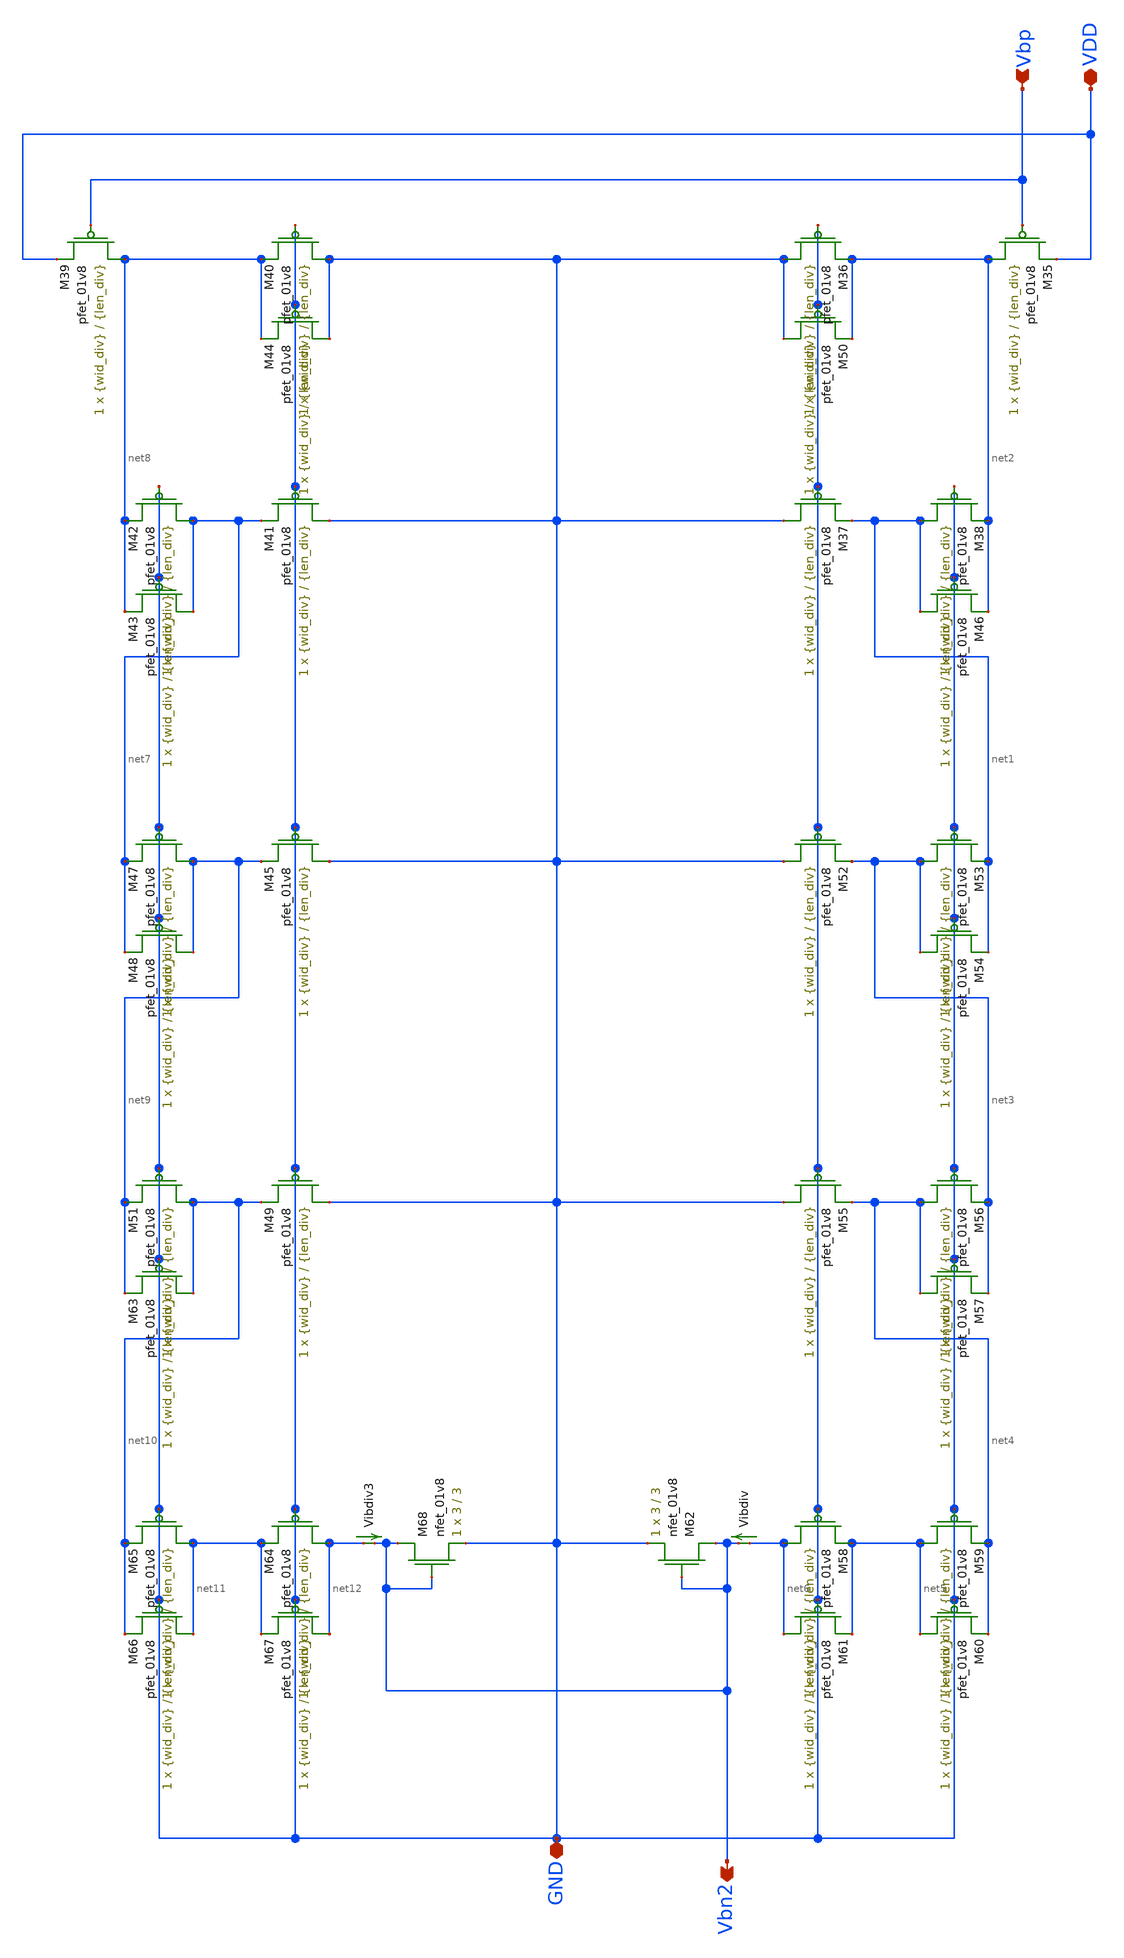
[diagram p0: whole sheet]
** sch_path: mp3/Layout_Schem_Designs/current_divider_lds.sch
**.subckt current_divider_lds Vbp VDD GND Vbn2
*.ipin Vbp
*.iopin VDD
*.iopin GND
*.opin Vbn2
XM35 net2 Vbp VDD VDD sky130_fd_pr__pfet_01v8 L={len_div} W={wid_div} nf=1 ad='int((nf+1)/2) * W/nf * 0.29'
+ as='int((nf+2)/2) * W/nf * 0.29' pd='2*int((nf+1)/2) * (W/nf + 0.29)' ps='2*int((nf+2)/2) * (W/nf + 0.29)'
+ nrd='0.29 / W' nrs='0.29 / W' sa=0 sb=0 sd=0 mult=1 m=1
XM36 GND GND net2 VDD sky130_fd_pr__pfet_01v8 L={len_div} W={wid_div} nf=1 ad='int((nf+1)/2) * W/nf * 0.29'
+ as='int((nf+2)/2) * W/nf * 0.29' pd='2*int((nf+1)/2) * (W/nf + 0.29)' ps='2*int((nf+2)/2) * (W/nf + 0.29)'
+ nrd='0.29 / W' nrs='0.29 / W' sa=0 sb=0 sd=0 mult=1 m=1
XM37 GND GND net1 VDD sky130_fd_pr__pfet_01v8 L={len_div} W={wid_div} nf=1 ad='int((nf+1)/2) * W/nf * 0.29'
+ as='int((nf+2)/2) * W/nf * 0.29' pd='2*int((nf+1)/2) * (W/nf + 0.29)' ps='2*int((nf+2)/2) * (W/nf + 0.29)'
+ nrd='0.29 / W' nrs='0.29 / W' sa=0 sb=0 sd=0 mult=1 m=1
XM38 net1 GND net2 VDD sky130_fd_pr__pfet_01v8 L={len_div} W={wid_div} nf=1 ad='int((nf+1)/2) * W/nf * 0.29'
+ as='int((nf+2)/2) * W/nf * 0.29' pd='2*int((nf+1)/2) * (W/nf + 0.29)' ps='2*int((nf+2)/2) * (W/nf + 0.29)'
+ nrd='0.29 / W' nrs='0.29 / W' sa=0 sb=0 sd=0 mult=1 m=1
XM46 net1 GND net2 VDD sky130_fd_pr__pfet_01v8 L={len_div} W={wid_div} nf=1 ad='int((nf+1)/2) * W/nf * 0.29'
+ as='int((nf+2)/2) * W/nf * 0.29' pd='2*int((nf+1)/2) * (W/nf + 0.29)' ps='2*int((nf+2)/2) * (W/nf + 0.29)'
+ nrd='0.29 / W' nrs='0.29 / W' sa=0 sb=0 sd=0 mult=1 m=1
XM50 GND GND net2 VDD sky130_fd_pr__pfet_01v8 L={len_div} W={wid_div} nf=1 ad='int((nf+1)/2) * W/nf * 0.29'
+ as='int((nf+2)/2) * W/nf * 0.29' pd='2*int((nf+1)/2) * (W/nf + 0.29)' ps='2*int((nf+2)/2) * (W/nf + 0.29)'
+ nrd='0.29 / W' nrs='0.29 / W' sa=0 sb=0 sd=0 mult=1 m=1
XM52 GND GND net3 VDD sky130_fd_pr__pfet_01v8 L={len_div} W={wid_div} nf=1 ad='int((nf+1)/2) * W/nf * 0.29'
+ as='int((nf+2)/2) * W/nf * 0.29' pd='2*int((nf+1)/2) * (W/nf + 0.29)' ps='2*int((nf+2)/2) * (W/nf + 0.29)'
+ nrd='0.29 / W' nrs='0.29 / W' sa=0 sb=0 sd=0 mult=1 m=1
XM53 net3 GND net1 VDD sky130_fd_pr__pfet_01v8 L={len_div} W={wid_div} nf=1 ad='int((nf+1)/2) * W/nf * 0.29'
+ as='int((nf+2)/2) * W/nf * 0.29' pd='2*int((nf+1)/2) * (W/nf + 0.29)' ps='2*int((nf+2)/2) * (W/nf + 0.29)'
+ nrd='0.29 / W' nrs='0.29 / W' sa=0 sb=0 sd=0 mult=1 m=1
XM54 net3 GND net1 VDD sky130_fd_pr__pfet_01v8 L={len_div} W={wid_div} nf=1 ad='int((nf+1)/2) * W/nf * 0.29'
+ as='int((nf+2)/2) * W/nf * 0.29' pd='2*int((nf+1)/2) * (W/nf + 0.29)' ps='2*int((nf+2)/2) * (W/nf + 0.29)'
+ nrd='0.29 / W' nrs='0.29 / W' sa=0 sb=0 sd=0 mult=1 m=1
XM55 GND GND net4 VDD sky130_fd_pr__pfet_01v8 L={len_div} W={wid_div} nf=1 ad='int((nf+1)/2) * W/nf * 0.29'
+ as='int((nf+2)/2) * W/nf * 0.29' pd='2*int((nf+1)/2) * (W/nf + 0.29)' ps='2*int((nf+2)/2) * (W/nf + 0.29)'
+ nrd='0.29 / W' nrs='0.29 / W' sa=0 sb=0 sd=0 mult=1 m=1
XM56 net4 GND net3 VDD sky130_fd_pr__pfet_01v8 L={len_div} W={wid_div} nf=1 ad='int((nf+1)/2) * W/nf * 0.29'
+ as='int((nf+2)/2) * W/nf * 0.29' pd='2*int((nf+1)/2) * (W/nf + 0.29)' ps='2*int((nf+2)/2) * (W/nf + 0.29)'
+ nrd='0.29 / W' nrs='0.29 / W' sa=0 sb=0 sd=0 mult=1 m=1
XM57 net4 GND net3 VDD sky130_fd_pr__pfet_01v8 L={len_div} W={wid_div} nf=1 ad='int((nf+1)/2) * W/nf * 0.29'
+ as='int((nf+2)/2) * W/nf * 0.29' pd='2*int((nf+1)/2) * (W/nf + 0.29)' ps='2*int((nf+2)/2) * (W/nf + 0.29)'
+ nrd='0.29 / W' nrs='0.29 / W' sa=0 sb=0 sd=0 mult=1 m=1
XM58 net6 GND net5 VDD sky130_fd_pr__pfet_01v8 L={len_div} W={wid_div} nf=1 ad='int((nf+1)/2) * W/nf * 0.29'
+ as='int((nf+2)/2) * W/nf * 0.29' pd='2*int((nf+1)/2) * (W/nf + 0.29)' ps='2*int((nf+2)/2) * (W/nf + 0.29)'
+ nrd='0.29 / W' nrs='0.29 / W' sa=0 sb=0 sd=0 mult=1 m=1
XM59 net5 GND net4 VDD sky130_fd_pr__pfet_01v8 L={len_div} W={wid_div} nf=1 ad='int((nf+1)/2) * W/nf * 0.29'
+ as='int((nf+2)/2) * W/nf * 0.29' pd='2*int((nf+1)/2) * (W/nf + 0.29)' ps='2*int((nf+2)/2) * (W/nf + 0.29)'
+ nrd='0.29 / W' nrs='0.29 / W' sa=0 sb=0 sd=0 mult=1 m=1
XM60 net5 GND net4 VDD sky130_fd_pr__pfet_01v8 L={len_div} W={wid_div} nf=1 ad='int((nf+1)/2) * W/nf * 0.29'
+ as='int((nf+2)/2) * W/nf * 0.29' pd='2*int((nf+1)/2) * (W/nf + 0.29)' ps='2*int((nf+2)/2) * (W/nf + 0.29)'
+ nrd='0.29 / W' nrs='0.29 / W' sa=0 sb=0 sd=0 mult=1 m=1
XM61 net6 GND net5 VDD sky130_fd_pr__pfet_01v8 L={len_div} W={wid_div} nf=1 ad='int((nf+1)/2) * W/nf * 0.29'
+ as='int((nf+2)/2) * W/nf * 0.29' pd='2*int((nf+1)/2) * (W/nf + 0.29)' ps='2*int((nf+2)/2) * (W/nf + 0.29)'
+ nrd='0.29 / W' nrs='0.29 / W' sa=0 sb=0 sd=0 mult=1 m=1
XM62 Vbn2 Vbn2 GND GND sky130_fd_pr__nfet_01v8 L=3 W=3 nf=1 ad='int((nf+1)/2) * W/nf * 0.29' as='int((nf+2)/2) * W/nf * 0.29'
+ pd='2*int((nf+1)/2) * (W/nf + 0.29)' ps='2*int((nf+2)/2) * (W/nf + 0.29)' nrd='0.29 / W' nrs='0.29 / W'
+ sa=0 sb=0 sd=0 mult=1 m=1
Vibdiv net6 Vbn2 0
.save i(vibdiv)
XM39 net8 Vbp VDD VDD sky130_fd_pr__pfet_01v8 L={len_div} W={wid_div} nf=1 ad='int((nf+1)/2) * W/nf * 0.29'
+ as='int((nf+2)/2) * W/nf * 0.29' pd='2*int((nf+1)/2) * (W/nf + 0.29)' ps='2*int((nf+2)/2) * (W/nf + 0.29)'
+ nrd='0.29 / W' nrs='0.29 / W' sa=0 sb=0 sd=0 mult=1 m=1
XM40 GND GND net8 VDD sky130_fd_pr__pfet_01v8 L={len_div} W={wid_div} nf=1 ad='int((nf+1)/2) * W/nf * 0.29'
+ as='int((nf+2)/2) * W/nf * 0.29' pd='2*int((nf+1)/2) * (W/nf + 0.29)' ps='2*int((nf+2)/2) * (W/nf + 0.29)'
+ nrd='0.29 / W' nrs='0.29 / W' sa=0 sb=0 sd=0 mult=1 m=1
XM41 GND GND net7 VDD sky130_fd_pr__pfet_01v8 L={len_div} W={wid_div} nf=1 ad='int((nf+1)/2) * W/nf * 0.29'
+ as='int((nf+2)/2) * W/nf * 0.29' pd='2*int((nf+1)/2) * (W/nf + 0.29)' ps='2*int((nf+2)/2) * (W/nf + 0.29)'
+ nrd='0.29 / W' nrs='0.29 / W' sa=0 sb=0 sd=0 mult=1 m=1
XM42 net7 GND net8 VDD sky130_fd_pr__pfet_01v8 L={len_div} W={wid_div} nf=1 ad='int((nf+1)/2) * W/nf * 0.29'
+ as='int((nf+2)/2) * W/nf * 0.29' pd='2*int((nf+1)/2) * (W/nf + 0.29)' ps='2*int((nf+2)/2) * (W/nf + 0.29)'
+ nrd='0.29 / W' nrs='0.29 / W' sa=0 sb=0 sd=0 mult=1 m=1
XM43 net7 GND net8 VDD sky130_fd_pr__pfet_01v8 L={len_div} W={wid_div} nf=1 ad='int((nf+1)/2) * W/nf * 0.29'
+ as='int((nf+2)/2) * W/nf * 0.29' pd='2*int((nf+1)/2) * (W/nf + 0.29)' ps='2*int((nf+2)/2) * (W/nf + 0.29)'
+ nrd='0.29 / W' nrs='0.29 / W' sa=0 sb=0 sd=0 mult=1 m=1
XM44 GND GND net8 VDD sky130_fd_pr__pfet_01v8 L={len_div} W={wid_div} nf=1 ad='int((nf+1)/2) * W/nf * 0.29'
+ as='int((nf+2)/2) * W/nf * 0.29' pd='2*int((nf+1)/2) * (W/nf + 0.29)' ps='2*int((nf+2)/2) * (W/nf + 0.29)'
+ nrd='0.29 / W' nrs='0.29 / W' sa=0 sb=0 sd=0 mult=1 m=1
XM45 GND GND net9 VDD sky130_fd_pr__pfet_01v8 L={len_div} W={wid_div} nf=1 ad='int((nf+1)/2) * W/nf * 0.29'
+ as='int((nf+2)/2) * W/nf * 0.29' pd='2*int((nf+1)/2) * (W/nf + 0.29)' ps='2*int((nf+2)/2) * (W/nf + 0.29)'
+ nrd='0.29 / W' nrs='0.29 / W' sa=0 sb=0 sd=0 mult=1 m=1
XM47 net9 GND net7 VDD sky130_fd_pr__pfet_01v8 L={len_div} W={wid_div} nf=1 ad='int((nf+1)/2) * W/nf * 0.29'
+ as='int((nf+2)/2) * W/nf * 0.29' pd='2*int((nf+1)/2) * (W/nf + 0.29)' ps='2*int((nf+2)/2) * (W/nf + 0.29)'
+ nrd='0.29 / W' nrs='0.29 / W' sa=0 sb=0 sd=0 mult=1 m=1
XM48 net9 GND net7 VDD sky130_fd_pr__pfet_01v8 L={len_div} W={wid_div} nf=1 ad='int((nf+1)/2) * W/nf * 0.29'
+ as='int((nf+2)/2) * W/nf * 0.29' pd='2*int((nf+1)/2) * (W/nf + 0.29)' ps='2*int((nf+2)/2) * (W/nf + 0.29)'
+ nrd='0.29 / W' nrs='0.29 / W' sa=0 sb=0 sd=0 mult=1 m=1
XM49 GND GND net10 VDD sky130_fd_pr__pfet_01v8 L={len_div} W={wid_div} nf=1 ad='int((nf+1)/2) * W/nf * 0.29'
+ as='int((nf+2)/2) * W/nf * 0.29' pd='2*int((nf+1)/2) * (W/nf + 0.29)' ps='2*int((nf+2)/2) * (W/nf + 0.29)'
+ nrd='0.29 / W' nrs='0.29 / W' sa=0 sb=0 sd=0 mult=1 m=1
XM51 net10 GND net9 VDD sky130_fd_pr__pfet_01v8 L={len_div} W={wid_div} nf=1 ad='int((nf+1)/2) * W/nf * 0.29'
+ as='int((nf+2)/2) * W/nf * 0.29' pd='2*int((nf+1)/2) * (W/nf + 0.29)' ps='2*int((nf+2)/2) * (W/nf + 0.29)'
+ nrd='0.29 / W' nrs='0.29 / W' sa=0 sb=0 sd=0 mult=1 m=1
XM63 net10 GND net9 VDD sky130_fd_pr__pfet_01v8 L={len_div} W={wid_div} nf=1 ad='int((nf+1)/2) * W/nf * 0.29'
+ as='int((nf+2)/2) * W/nf * 0.29' pd='2*int((nf+1)/2) * (W/nf + 0.29)' ps='2*int((nf+2)/2) * (W/nf + 0.29)'
+ nrd='0.29 / W' nrs='0.29 / W' sa=0 sb=0 sd=0 mult=1 m=1
XM64 net12 GND net11 VDD sky130_fd_pr__pfet_01v8 L={len_div} W={wid_div} nf=1 ad='int((nf+1)/2) * W/nf * 0.29'
+ as='int((nf+2)/2) * W/nf * 0.29' pd='2*int((nf+1)/2) * (W/nf + 0.29)' ps='2*int((nf+2)/2) * (W/nf + 0.29)'
+ nrd='0.29 / W' nrs='0.29 / W' sa=0 sb=0 sd=0 mult=1 m=1
XM65 net11 GND net10 VDD sky130_fd_pr__pfet_01v8 L={len_div} W={wid_div} nf=1 ad='int((nf+1)/2) * W/nf * 0.29'
+ as='int((nf+2)/2) * W/nf * 0.29' pd='2*int((nf+1)/2) * (W/nf + 0.29)' ps='2*int((nf+2)/2) * (W/nf + 0.29)'
+ nrd='0.29 / W' nrs='0.29 / W' sa=0 sb=0 sd=0 mult=1 m=1
XM66 net11 GND net10 VDD sky130_fd_pr__pfet_01v8 L={len_div} W={wid_div} nf=1 ad='int((nf+1)/2) * W/nf * 0.29'
+ as='int((nf+2)/2) * W/nf * 0.29' pd='2*int((nf+1)/2) * (W/nf + 0.29)' ps='2*int((nf+2)/2) * (W/nf + 0.29)'
+ nrd='0.29 / W' nrs='0.29 / W' sa=0 sb=0 sd=0 mult=1 m=1
XM67 net12 GND net11 VDD sky130_fd_pr__pfet_01v8 L={len_div} W={wid_div} nf=1 ad='int((nf+1)/2) * W/nf * 0.29'
+ as='int((nf+2)/2) * W/nf * 0.29' pd='2*int((nf+1)/2) * (W/nf + 0.29)' ps='2*int((nf+2)/2) * (W/nf + 0.29)'
+ nrd='0.29 / W' nrs='0.29 / W' sa=0 sb=0 sd=0 mult=1 m=1
XM68 Vbn2 Vbn2 GND GND sky130_fd_pr__nfet_01v8 L=3 W=3 nf=1 ad='int((nf+1)/2) * W/nf * 0.29' as='int((nf+2)/2) * W/nf * 0.29'
+ pd='2*int((nf+1)/2) * (W/nf + 0.29)' ps='2*int((nf+2)/2) * (W/nf + 0.29)' nrd='0.29 / W' nrs='0.29 / W'
+ sa=0 sb=0 sd=0 mult=1 m=1
Vibdiv3 net12 Vbn2 0
.save i(vibdiv3)
**** begin user architecture code

.param len_div=4 wid_div=3 len=4 wid=3

**** end user architecture code
**.ends
.end
